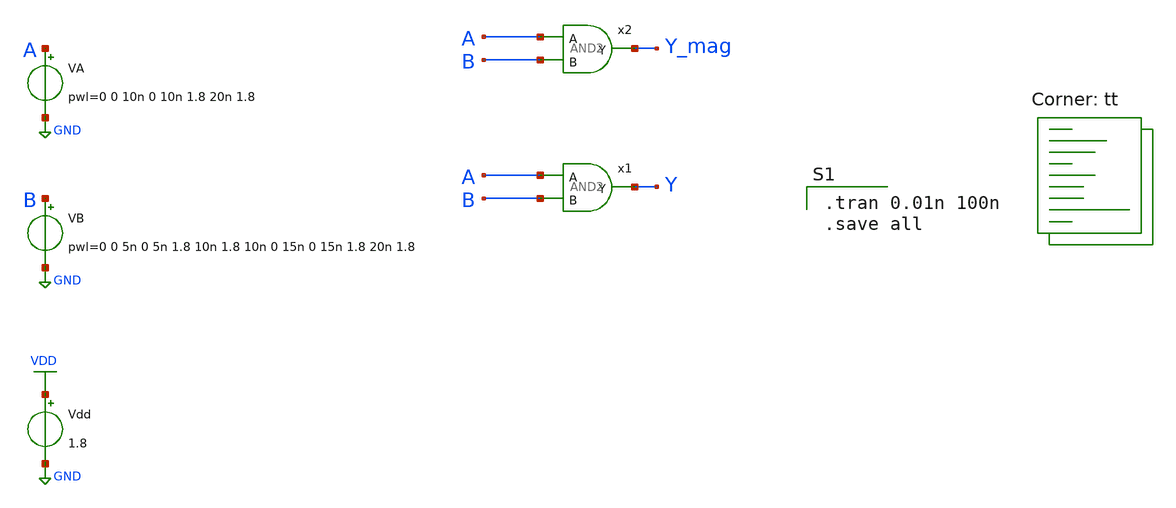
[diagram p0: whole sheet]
** sch_path: gates/AND2SIMSYM.sch
**.subckt AND2SIMSYM
Vdd VDD GND 1.8
VA A GND pwl=0 0 10n 0 10n 1.8 20n 1.8
VB B GND pwl=0 0 5n 0 5n 1.8 10n 1.8 10n 0 15n 0 15n 1.8 20n 1.8
x1 A Y B AND2
x2 A Y_mag B AND_Gate_parax
**** begin user architecture code

.tran 0.01n 100n
.save all

.lib $::SKYWATER_MODELS/sky130.lib.spice tt
**** end user architecture code
**.ends

* expanding   symbol:  AND2.sym # of pins=3
** sym_path: gates/AND2.sym
** sch_path: gates/AND2.sch
.subckt AND2 A Y B
*.opin Y
*.ipin A
*.ipin B
x1 A net1 B NAND2_Gate
X2 net1 Y inv_vtc
.ends


* expanding   symbol:  AND_Gate_parax.sym # of pins=3
** sym_path: gates/AND2.sym
.include [file normalize /home/apn/mag_gates/AND_Gate_parax.spice]

* expanding   symbol:  NAND2_Gate.sym # of pins=3
** sym_path: gates/NAND2_Gate.sym
** sch_path: gates/NAND2_Gate.sch
.subckt NAND2_Gate A Y B
*.ipin A
*.ipin B
*.opin Y
XM1 Y A net1 GND sky130_fd_pr__nfet_01v8 L=0.15 W=1 nf=1 ad='int((nf+1)/2) * W/nf * 0.29' as='int((nf+2)/2) * W/nf * 0.29'
+ pd='2*int((nf+1)/2) * (W/nf + 0.29)' ps='2*int((nf+2)/2) * (W/nf + 0.29)' nrd='0.29 / W' nrs='0.29 / W'
+ sa=0 sb=0 sd=0 mult=1 m=1
XM2 net1 B GND GND sky130_fd_pr__nfet_01v8 L=0.15 W=1 nf=1 ad='int((nf+1)/2) * W/nf * 0.29' as='int((nf+2)/2) * W/nf * 0.29'
+ pd='2*int((nf+1)/2) * (W/nf + 0.29)' ps='2*int((nf+2)/2) * (W/nf + 0.29)' nrd='0.29 / W' nrs='0.29 / W'
+ sa=0 sb=0 sd=0 mult=1 m=1
XM3 Y A VDD VDD sky130_fd_pr__pfet_01v8 L=0.15 W=1 nf=1 ad='int((nf+1)/2) * W/nf * 0.29' as='int((nf+2)/2) * W/nf * 0.29'
+ pd='2*int((nf+1)/2) * (W/nf + 0.29)' ps='2*int((nf+2)/2) * (W/nf + 0.29)' nrd='0.29 / W' nrs='0.29 / W'
+ sa=0 sb=0 sd=0 mult=1 m=1
XM4 Y B VDD VDD sky130_fd_pr__pfet_01v8 L=0.15 W=1 nf=1 ad='int((nf+1)/2) * W/nf * 0.29' as='int((nf+2)/2) * W/nf * 0.29'
+ pd='2*int((nf+1)/2) * (W/nf + 0.29)' ps='2*int((nf+2)/2) * (W/nf + 0.29)' nrd='0.29 / W' nrs='0.29 / W'
+ sa=0 sb=0 sd=0 mult=1 m=1
.ends


* expanding   symbol:  /home/apn/test_xschem_sky130/inv_vtc.sym # of pins=2
** sym_path: gates/inv_vtc.sym
** sch_path: gates/inv_vtc.sch
.subckt inv_vtc A Y
*.ipin A
*.opin Y
XM1 Y A VDD VDD sky130_fd_pr__pfet_01v8 L=0.15 W=2 nf=1 ad='int((nf+1)/2) * W/nf * 0.29' as='int((nf+2)/2) * W/nf * 0.29'
+ pd='2*int((nf+1)/2) * (W/nf + 0.29)' ps='2*int((nf+2)/2) * (W/nf + 0.29)' nrd='0.29 / W' nrs='0.29 / W'
+ sa=0 sb=0 sd=0 mult=1 m=1
XM2 Y A GND GND sky130_fd_pr__nfet_01v8 L=0.15 W=1 nf=1 ad='int((nf+1)/2) * W/nf * 0.29' as='int((nf+2)/2) * W/nf * 0.29'
+ pd='2*int((nf+1)/2) * (W/nf + 0.29)' ps='2*int((nf+2)/2) * (W/nf + 0.29)' nrd='0.29 / W' nrs='0.29 / W'
+ sa=0 sb=0 sd=0 mult=1 m=1
.ends

.GLOBAL VDD
.GLOBAL GND
.end
